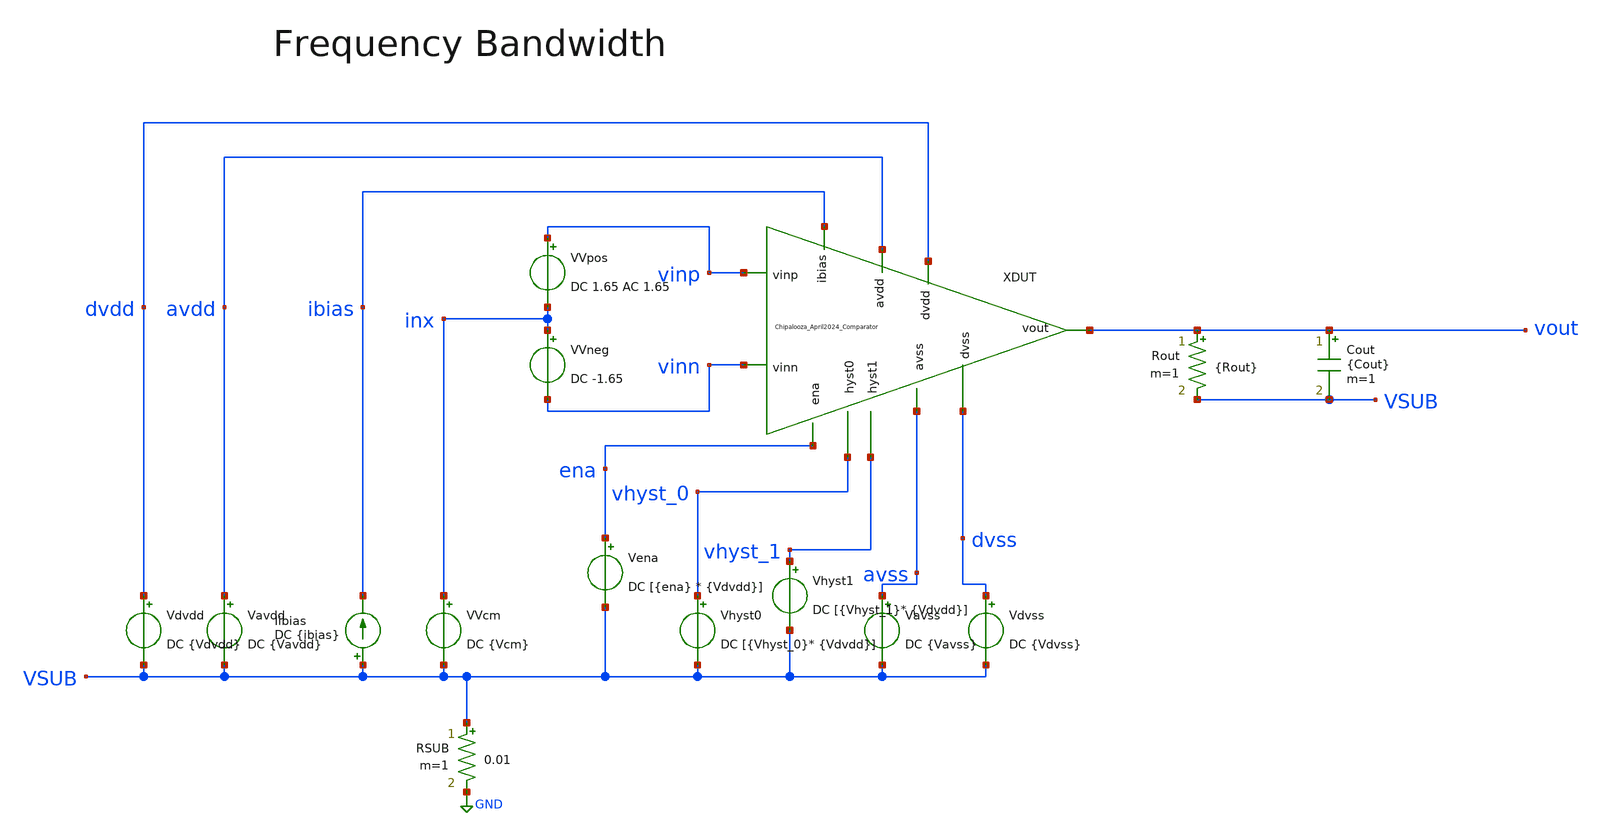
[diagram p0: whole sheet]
** sch_path: Chipalooza_April2024_Comparator/xschem/TB_frequencyBandwidth.sch
**.subckt TB_frequencyBandwidth
Vavdd avdd VSUB DC {Vavdd}
Rout vout VSUB {Rout} m=1
Cout vout VSUB {Cout} m=1
Vdvdd dvdd VSUB DC {Vdvdd}
Vena ena VSUB DC [{ena} * {Vdvdd}]
Vhyst0 vhyst_0 VSUB DC [{Vhyst_0}* {Vdvdd}]
Vhyst1 vhyst_1 VSUB DC [{Vhyst_1}* {Vdvdd}]
Vavss avss VSUB DC {Vavss}
Vdvss dvss VSUB DC {Vdvss}
RSUB VSUB GND 0.01 m=1
Iibias VSUB ibias DC {ibias}
XDUT vhyst_0 vhyst_1 avdd vinp avss vinn dvdd dvss vout ibias ena Chipalooza_April2024_Comparator
VVpos vinp inx DC 1.65 AC 1.65
VVneg inx vinn DC -1.65
VVcm inx VSUB DC {Vcm}
**** begin user architecture code

.control

ac dec 20 1 1e12
plot v(vout)
plot v(dvdd)
plot v(avdd)

meas ac peak MAX vmag(vout) FROM=2 TO=1.5GHz
let f3db = peak/sqrt(2)
meas ac f1 when vmag(vout)=f3db RISE=1
meas ac f2 when vmag(vout)=f3db FALL=1

let f3 = $&f2
echo $&f3 > {simpath}/{filename}_{N}.data

write ngspice/frequencyBandwidth.raw

.endc



* CACE gensim simulation file {filename}_{N}
* Generated by CACE gensim, Efabless Corporation (c) 2023
* Find the current through the amplifier under condition of static input

.include {DUT_path}

.lib {PDK_ROOT}/{PDK}/libs.tech/combined/sky130.lib.spice {corner}

.option TEMP={temperature}
* Flag unsafe operating conditions (exceeds models' specified limits)
.option warn=1
.option savecurrents
.option save all


**** end user architecture code
**.ends

* expanding   symbol:  Chipalooza_April2024_Comparator.sym # of pins=11
** sym_path: Chipalooza_April2024_Comparator/xschem/Chipalooza_April2024_Comparator.sym
** sch_path: Chipalooza_April2024_Comparator/xschem/Chipalooza_April2024_Comparator.sch
.subckt Chipalooza_April2024_Comparator hyst0 hyst1 avdd vinp avss vinn dvdd dvss vout ibias ena
*.ipin vinp
*.ipin vinn
*.ipin hyst0
*.ipin hyst1
*.ipin avdd
*.ipin avss
*.ipin dvdd
*.ipin dvss
*.opin vout
*.ipin ena
*.ipin ibias
XM29 SumOutBar SumOut dvdd dvdd sky130_fd_pr__pfet_01v8 L=1 W=2 nf=1 ad='int((nf+1)/2) * W/nf * 0.29' as='int((nf+2)/2)
+ * W/nf * 0.29' pd='2*int((nf+1)/2) * (W/nf + 0.29)' ps='2*int((nf+2)/2) * (W/nf + 0.29)' nrd='0.29 /
+ W' nrs='0.29 / W' sa=0 sb=0 sd=0 mult=2 m=2
XM30 SumOutBar SumOut dvssi dvss sky130_fd_pr__nfet_01v8 L=1 W=2 nf=1 ad='int((nf+1)/2) * W/nf * 0.29' as='int((nf+2)/2)
+ * W/nf * 0.29' pd='2*int((nf+1)/2) * (W/nf + 0.29)' ps='2*int((nf+2)/2) * (W/nf + 0.29)' nrd='0.29 /
+ W' nrs='0.29 / W' sa=0 sb=0 sd=0 mult=2 m=2
XM25 net2 hyst_bias0 avss avss sky130_fd_pr__nfet_g5v0d10v5 L=1 W=3 nf=1 ad='int((nf+1)/2) * W/nf * 0.29' as='int((nf+2)/2)
+ * W/nf * 0.29' pd='2*int((nf+1)/2) * (W/nf + 0.29)' ps='2*int((nf+2)/2) * (W/nf + 0.29)' nrd='0.29 /
+ W' nrs='0.29 / W' sa=0 sb=0 sd=0 mult=2 m=2
XM26 hyst_bias0 ibias dvssi dvss sky130_fd_pr__nfet_01v8 L=1 W=3 nf=1 ad='int((1 + 1)/2) * 3 / 1 * 0.29' as='int((1
+ + 2)/2) * 3 / 1 * 0.29' pd='2*int((1 + 1)/2) * (3 / 1 + 0.29)' ps='2*int((1 + 2)/2) * (3 / 1 + 0.29)' nrd='0.29
+ / 3 ' nrs='0.29 / 3 ' sa=0 sb=0 sd=0 mult=2 m=2
XM27 ibias ibias dvssi dvss sky130_fd_pr__nfet_01v8 L=1 W=3 nf=1 ad='int((1 + 1)/2) * 3 / 1 * 0.29' as='int((1
+ + 2)/2) * 3 / 1 * 0.29' pd='2*int((1 + 1)/2) * (3 / 1 + 0.29)' ps='2*int((1 + 2)/2) * (3 / 1 + 0.29)' nrd='0.29
+ / 3 ' nrs='0.29 / 3 ' sa=0 sb=0 sd=0 mult=2 m=2
XM34 hyst_bias1 hyst_bias0 dvdd dvdd sky130_fd_pr__pfet_01v8 L=1 W=3 nf=1 ad='int((nf+1)/2) * W/nf *
+ 0.29' as='int((nf+2)/2) * W/nf * 0.29' pd='2*int((nf+1)/2) * (W/nf + 0.29)' ps='2*int((nf+2)/2) * (W/nf
+ + 0.29)' nrd='0.29 / W' nrs='0.29 / W' sa=0 sb=0 sd=0 mult=2 m=2
XM35 hyst_bias0 hyst_bias0 dvdd dvdd sky130_fd_pr__pfet_01v8 L=1 W=3 nf=1 ad='int((nf+1)/2) * W/nf *
+ 0.29' as='int((nf+2)/2) * W/nf * 0.29' pd='2*int((nf+1)/2) * (W/nf + 0.29)' ps='2*int((nf+2)/2) * (W/nf
+ + 0.29)' nrd='0.29 / W' nrs='0.29 / W' sa=0 sb=0 sd=0 mult=2 m=2
XM36 dvdd hyst_bias1 dvssi dvss sky130_fd_pr__nfet_01v8 L=1 W=3 nf=1 ad='int((1 + 1)/2) * 3 / 1 * 0.29' as='int((1
+ + 2)/2) * 3 / 1 * 0.29' pd='2*int((1 + 1)/2) * (3 / 1 + 0.29)' ps='2*int((1 + 2)/2) * (3 / 1 + 0.29)' nrd='0.29
+ / 3 ' nrs='0.29 / 3 ' sa=0 sb=0 sd=0 mult=2 m=2
XM37 hyst_bias1 hyst_bias1 dvssi dvss sky130_fd_pr__nfet_01v8 L=1 W=3 nf=1 ad='int((1 + 1)/2) * 3 / 1
+ * 0.29' as='int((1 + 2)/2) * 3 / 1 * 0.29' pd='2*int((1 + 1)/2) * (3 / 1 + 0.29)' ps='2*int((1 + 2)/2)
+ * (3 / 1 + 0.29)' nrd='0.29 / 3 ' nrs='0.29 / 3 ' sa=0 sb=0 sd=0 mult=2 m=2
C1 avss 0 2p m=1
XM38 avssi ena avss avss sky130_fd_pr__nfet_g5v0d10v5 L=1 W=16 nf=1 ad='int((nf+1)/2) * W/nf * 0.29' as='int((nf+2)/2)
+ * W/nf * 0.29' pd='2*int((nf+1)/2) * (W/nf + 0.29)' ps='2*int((nf+2)/2) * (W/nf + 0.29)' nrd='0.29 /
+ W' nrs='0.29 / W' sa=0 sb=0 sd=0 mult=2 m=2
XM39 net3 hyst_bias0 avss avss sky130_fd_pr__nfet_g5v0d10v5 L=1 W=8 nf=1 ad='int((nf+1)/2) * W/nf * 0.29' as='int((nf+2)/2)
+ * W/nf * 0.29' pd='2*int((nf+1)/2) * (W/nf + 0.29)' ps='2*int((nf+2)/2) * (W/nf + 0.29)' nrd='0.29 /
+ W' nrs='0.29 / W' sa=0 sb=0 sd=0 mult=4 m=4
XM40 net1 hyst0 net2 avss sky130_fd_pr__nfet_g5v0d10v5 L=1 W=3 nf=1 ad='int((nf+1)/2) * W/nf * 0.29' as='int((nf+2)/2)
+ * W/nf * 0.29' pd='2*int((nf+1)/2) * (W/nf + 0.29)' ps='2*int((nf+2)/2) * (W/nf + 0.29)' nrd='0.29 /
+ W' nrs='0.29 / W' sa=0 sb=0 sd=0 mult=2 m=2
XM41 net1 hyst1 net3 avss sky130_fd_pr__nfet_g5v0d10v5 L=1 W=8 nf=1 ad='int((nf+1)/2) * W/nf * 0.29' as='int((nf+2)/2)
+ * W/nf * 0.29' pd='2*int((nf+1)/2) * (W/nf + 0.29)' ps='2*int((nf+2)/2) * (W/nf + 0.29)' nrd='0.29 /
+ W' nrs='0.29 / W' sa=0 sb=0 sd=0 mult=4 m=4
C2 avss 0 2p m=1
XM13 dvssi ena avss avss sky130_fd_pr__nfet_g5v0d10v5 L=1 W=16 nf=1 ad='int((nf+1)/2) * W/nf * 0.29' as='int((nf+2)/2)
+ * W/nf * 0.29' pd='2*int((nf+1)/2) * (W/nf + 0.29)' ps='2*int((nf+2)/2) * (W/nf + 0.29)' nrd='0.29 /
+ W' nrs='0.29 / W' sa=0 sb=0 sd=0 mult=2 m=2
XM16 vout SumOutBar dvdd dvdd sky130_fd_pr__pfet_01v8 L=1 W=2 nf=1 ad='int((nf+1)/2) * W/nf * 0.29' as='int((nf+2)/2)
+ * W/nf * 0.29' pd='2*int((nf+1)/2) * (W/nf + 0.29)' ps='2*int((nf+2)/2) * (W/nf + 0.29)' nrd='0.29 /
+ W' nrs='0.29 / W' sa=0 sb=0 sd=0 mult=2 m=2
XM18 vout SumOutBar dvssi dvss sky130_fd_pr__nfet_01v8 L=1 W=2 nf=1 ad='int((nf+1)/2) * W/nf * 0.29' as='int((nf+2)/2)
+ * W/nf * 0.29' pd='2*int((nf+1)/2) * (W/nf + 0.29)' ps='2*int((nf+2)/2) * (W/nf + 0.29)' nrd='0.29 /
+ W' nrs='0.29 / W' sa=0 sb=0 sd=0 mult=2 m=2
XM19 net14 SumOutBar net15 dvdd sky130_fd_pr__pfet_01v8 L=1 W=2 nf=1 ad='int((nf+1)/2) * W/nf * 0.29' as='int((nf+2)/2)
+ * W/nf * 0.29' pd='2*int((nf+1)/2) * (W/nf + 0.29)' ps='2*int((nf+2)/2) * (W/nf + 0.29)' nrd='0.29 /
+ W' nrs='0.29 / W' sa=0 sb=0 sd=0 mult=2 m=2
XM24 net1 SumOut N2 dvdd sky130_fd_pr__pfet_01v8 L=1 W=2 nf=1 ad='int((nf+1)/2) * W/nf * 0.29' as='int((nf+2)/2)
+ * W/nf * 0.29' pd='2*int((nf+1)/2) * (W/nf + 0.29)' ps='2*int((nf+2)/2) * (W/nf + 0.29)' nrd='0.29 /
+ W' nrs='0.29 / W' sa=0 sb=0 sd=0 mult=2 m=2
XM4 SourceBias2 SourceBias2 avdd avdd sky130_fd_pr__pfet_g5v0d10v5 L=1 W=2 nf=1 ad='int((nf+1)/2) * W/nf
+ * 0.29' as='int((nf+2)/2) * W/nf * 0.29' pd='2*int((nf+1)/2) * (W/nf + 0.29)' ps='2*int((nf+2)/2) * (W/nf
+ + 0.29)' nrd='0.29 / W' nrs='0.29 / W' sa=0 sb=0 sd=0 mult=2 m=2
XM5 N1 SourceBias2 avdd avdd sky130_fd_pr__pfet_g5v0d10v5 L=1 W=2 nf=1 ad='int((nf+1)/2) * W/nf * 0.29' as='int((nf+2)/2)
+ * W/nf * 0.29' pd='2*int((nf+1)/2) * (W/nf + 0.29)' ps='2*int((nf+2)/2) * (W/nf + 0.29)' nrd='0.29 /
+ W' nrs='0.29 / W' sa=0 sb=0 sd=0 mult=2 m=2
XM6 N2 SourceBias2 avdd avdd sky130_fd_pr__pfet_g5v0d10v5 L=1 W=2 nf=1 ad='int((nf+1)/2) * W/nf * 0.29' as='int((nf+2)/2)
+ * W/nf * 0.29' pd='2*int((nf+1)/2) * (W/nf + 0.29)' ps='2*int((nf+2)/2) * (W/nf + 0.29)' nrd='0.29 /
+ W' nrs='0.29 / W' sa=0 sb=0 sd=0 mult=2 m=2
XM7 SumOut Bias1 N2 avdd sky130_fd_pr__pfet_g5v0d10v5 L=1 W=2 nf=1 ad='int((nf+1)/2) * W/nf * 0.29' as='int((nf+2)/2)
+ * W/nf * 0.29' pd='2*int((nf+1)/2) * (W/nf + 0.29)' ps='2*int((nf+2)/2) * (W/nf + 0.29)' nrd='0.29 /
+ W' nrs='0.29 / W' sa=0 sb=0 sd=0 mult=2 m=2
XM8 Sum Bias1 N1 avdd sky130_fd_pr__pfet_g5v0d10v5 L=1 W=2 nf=1 ad='int((nf+1)/2) * W/nf * 0.29' as='int((nf+2)/2)
+ * W/nf * 0.29' pd='2*int((nf+1)/2) * (W/nf + 0.29)' ps='2*int((nf+2)/2) * (W/nf + 0.29)' nrd='0.29 /
+ W' nrs='0.29 / W' sa=0 sb=0 sd=0 mult=2 m=2
XM9 SumOut Bias2 P2 avss sky130_fd_pr__nfet_g5v0d10v5 L=1 W=2 nf=1 ad='int((nf+1)/2) * W/nf * 0.29' as='int((nf+2)/2)
+ * W/nf * 0.29' pd='2*int((nf+1)/2) * (W/nf + 0.29)' ps='2*int((nf+2)/2) * (W/nf + 0.29)' nrd='0.29 /
+ W' nrs='0.29 / W' sa=0 sb=0 sd=0 mult=2 m=2
XM10 Sum Bias2 P1 avss sky130_fd_pr__nfet_g5v0d10v5 L=1 W=2 nf=1 ad='int((nf+1)/2) * W/nf * 0.29' as='int((nf+2)/2)
+ * W/nf * 0.29' pd='2*int((nf+1)/2) * (W/nf + 0.29)' ps='2*int((nf+2)/2) * (W/nf + 0.29)' nrd='0.29 /
+ W' nrs='0.29 / W' sa=0 sb=0 sd=0 mult=2 m=2
XM11 P2 Sum avss avss sky130_fd_pr__nfet_g5v0d10v5 L=1 W=2 nf=1 ad='int((nf+1)/2) * W/nf * 0.29' as='int((nf+2)/2)
+ * W/nf * 0.29' pd='2*int((nf+1)/2) * (W/nf + 0.29)' ps='2*int((nf+2)/2) * (W/nf + 0.29)' nrd='0.29 /
+ W' nrs='0.29 / W' sa=0 sb=0 sd=0 mult=2 m=2
XM12 P1 Sum avss avss sky130_fd_pr__nfet_g5v0d10v5 L=1 W=2 nf=1 ad='int((nf+1)/2) * W/nf * 0.29' as='int((nf+2)/2)
+ * W/nf * 0.29' pd='2*int((nf+1)/2) * (W/nf + 0.29)' ps='2*int((nf+2)/2) * (W/nf + 0.29)' nrd='0.29 /
+ W' nrs='0.29 / W' sa=0 sb=0 sd=0 mult=2 m=2
XM2 P2 vinn psource_input avdd sky130_fd_pr__pfet_g5v0d10v5 L=1 W=4 nf=1 ad='int((nf+1)/2) * W/nf * 0.29' as='int((nf+2)/2)
+ * W/nf * 0.29' pd='2*int((nf+1)/2) * (W/nf + 0.29)' ps='2*int((nf+2)/2) * (W/nf + 0.29)' nrd='0.29 /
+ W' nrs='0.29 / W' sa=0 sb=0 sd=0 mult=2 m=2
XM3 P1 vinp psource_input avdd sky130_fd_pr__pfet_g5v0d10v5 L=1 W=4 nf=1 ad='int((nf+1)/2) * W/nf * 0.29' as='int((nf+2)/2)
+ * W/nf * 0.29' pd='2*int((nf+1)/2) * (W/nf + 0.29)' ps='2*int((nf+2)/2) * (W/nf + 0.29)' nrd='0.29 /
+ W' nrs='0.29 / W' sa=0 sb=0 sd=0 mult=2 m=2
XM14 psource_input net4 avdd avdd sky130_fd_pr__pfet_g5v0d10v5 L=1 W=12 nf=1 ad='int((nf+1)/2) * W/nf
+ * 0.29' as='int((nf+2)/2) * W/nf * 0.29' pd='2*int((nf+1)/2) * (W/nf + 0.29)' ps='2*int((nf+2)/2) * (W/nf
+ + 0.29)' nrd='0.29 / W' nrs='0.29 / W' sa=0 sb=0 sd=0 mult=4 m=4
XM15 net4 net4 avdd avdd sky130_fd_pr__pfet_g5v0d10v5 L=1 W=8 nf=1 ad='int((nf+1)/2) * W/nf * 0.29' as='int((nf+2)/2)
+ * W/nf * 0.29' pd='2*int((nf+1)/2) * (W/nf + 0.29)' ps='2*int((nf+2)/2) * (W/nf + 0.29)' nrd='0.29 /
+ W' nrs='0.29 / W' sa=0 sb=0 sd=0 mult=2 m=2
XM17 nbias_tail net6 psource_input avdd sky130_fd_pr__pfet_g5v0d10v5 L=1 W=8 nf=1 ad='int((nf+1)/2) *
+ W/nf * 0.29' as='int((nf+2)/2) * W/nf * 0.29' pd='2*int((nf+1)/2) * (W/nf + 0.29)' ps='2*int((nf+2)/2)
+ * (W/nf + 0.29)' nrd='0.29 / W' nrs='0.29 / W' sa=0 sb=0 sd=0 mult=2 m=2
XM20 N1 vinp SourceBias0 avss sky130_fd_pr__nfet_g5v0d10v5 L=4 W=16 nf=1 ad='int((nf+1)/2) * W/nf * 0.29' as='int((nf+2)/2)
+ * W/nf * 0.29' pd='2*int((nf+1)/2) * (W/nf + 0.29)' ps='2*int((nf+2)/2) * (W/nf + 0.29)' nrd='0.29 /
+ W' nrs='0.29 / W' sa=0 sb=0 sd=0 mult=2 m=2
XM21 N2 vinn SourceBias0 avss sky130_fd_pr__nfet_g5v0d10v5 L=4 W=16 nf=1 ad='int((nf+1)/2) * W/nf * 0.29' as='int((nf+2)/2)
+ * W/nf * 0.29' pd='2*int((nf+1)/2) * (W/nf + 0.29)' ps='2*int((nf+2)/2) * (W/nf + 0.29)' nrd='0.29 /
+ W' nrs='0.29 / W' sa=0 sb=0 sd=0 mult=2 m=2
XM22 SourceBias0 nbias_tail avssi avss sky130_fd_pr__nfet_g5v0d10v5 L=1 W=12 nf=1 ad='int((nf+1)/2) *
+ W/nf * 0.29' as='int((nf+2)/2) * W/nf * 0.29' pd='2*int((nf+1)/2) * (W/nf + 0.29)' ps='2*int((nf+2)/2)
+ * (W/nf + 0.29)' nrd='0.29 / W' nrs='0.29 / W' sa=0 sb=0 sd=0 mult=4 m=4
XM23 nbias_tail nbias_tail avssi avss sky130_fd_pr__nfet_g5v0d10v5 L=1 W=12 nf=1 ad='int((nf+1)/2) *
+ W/nf * 0.29' as='int((nf+2)/2) * W/nf * 0.29' pd='2*int((nf+1)/2) * (W/nf + 0.29)' ps='2*int((nf+2)/2)
+ * (W/nf + 0.29)' nrd='0.29 / W' nrs='0.29 / W' sa=0 sb=0 sd=0 mult=2 m=2
XM28 net4 Bias5 SourceBias0 avss sky130_fd_pr__nfet_g5v0d10v5 L=1 W=4 nf=1 ad='int((nf+1)/2) * W/nf *
+ 0.29' as='int((nf+2)/2) * W/nf * 0.29' pd='2*int((nf+1)/2) * (W/nf + 0.29)' ps='2*int((nf+2)/2) * (W/nf
+ + 0.29)' nrd='0.29 / W' nrs='0.29 / W' sa=0 sb=0 sd=0 mult=2 m=2
XM31 SourceBias0 net5 avssi avss sky130_fd_pr__nfet_g5v0d10v5 L=4 W=16 nf=1 ad='int((nf+1)/2) * W/nf
+ * 0.29' as='int((nf+2)/2) * W/nf * 0.29' pd='2*int((nf+1)/2) * (W/nf + 0.29)' ps='2*int((nf+2)/2) * (W/nf
+ + 0.29)' nrd='0.29 / W' nrs='0.29 / W' sa=0 sb=0 sd=0 mult=2 m=2
XM44 net5 net5 avssi avss sky130_fd_pr__nfet_g5v0d10v5 L=4 W=16 nf=1 ad='int((nf+1)/2) * W/nf * 0.29' as='int((nf+2)/2)
+ * W/nf * 0.29' pd='2*int((nf+1)/2) * (W/nf + 0.29)' ps='2*int((nf+2)/2) * (W/nf + 0.29)' nrd='0.29 /
+ W' nrs='0.29 / W' sa=0 sb=0 sd=0 mult=2 m=2
XM45 SourceBias1 net5 avssi avss sky130_fd_pr__nfet_g5v0d10v5 L=4 W=16 nf=1 ad='int((nf+1)/2) * W/nf
+ * 0.29' as='int((nf+2)/2) * W/nf * 0.29' pd='2*int((nf+1)/2) * (W/nf + 0.29)' ps='2*int((nf+2)/2) * (W/nf
+ + 0.29)' nrd='0.29 / W' nrs='0.29 / W' sa=0 sb=0 sd=0 mult=2 m=2
XM46 SourceBias1 SourceBias1 avdd avdd sky130_fd_pr__pfet_g5v0d10v5 L=1 W=12 nf=1 ad='int((nf+1)/2) *
+ W/nf * 0.29' as='int((nf+2)/2) * W/nf * 0.29' pd='2*int((nf+1)/2) * (W/nf + 0.29)' ps='2*int((nf+2)/2)
+ * (W/nf + 0.29)' nrd='0.29 / W' nrs='0.29 / W' sa=0 sb=0 sd=0 mult=4 m=4
XM47 psource_input SourceBias1 avdd avdd sky130_fd_pr__pfet_g5v0d10v5 L=1 W=12 nf=1 ad='int((nf+1)/2)
+ * W/nf * 0.29' as='int((nf+2)/2) * W/nf * 0.29' pd='2*int((nf+1)/2) * (W/nf + 0.29)' ps='2*int((nf+2)/2)
+ * (W/nf + 0.29)' nrd='0.29 / W' nrs='0.29 / W' sa=0 sb=0 sd=0 mult=4 m=4
XM48 SourceBias2 net5 avssi avss sky130_fd_pr__nfet_g5v0d10v5 L=4 W=16 nf=1 ad='int((nf+1)/2) * W/nf
+ * 0.29' as='int((nf+2)/2) * W/nf * 0.29' pd='2*int((nf+1)/2) * (W/nf + 0.29)' ps='2*int((nf+2)/2) * (W/nf
+ + 0.29)' nrd='0.29 / W' nrs='0.29 / W' sa=0 sb=0 sd=0 mult=4 m=4
XM63 net6 net6 avdd avdd sky130_fd_pr__pfet_g5v0d10v5 L=5 W=3 nf=1 ad='int((nf+1)/2) * W/nf * 0.29' as='int((nf+2)/2)
+ * W/nf * 0.29' pd='2*int((nf+1)/2) * (W/nf + 0.29)' ps='2*int((nf+2)/2) * (W/nf + 0.29)' nrd='0.29 /
+ W' nrs='0.29 / W' sa=0 sb=0 sd=0 mult=1 m=1
XM62 avdd Bias4 SourceBias3 avss sky130_fd_pr__nfet_g5v0d10v5 L=1 W=4 nf=1 ad='int((nf+1)/2) * W/nf *
+ 0.29' as='int((nf+2)/2) * W/nf * 0.29' pd='2*int((nf+1)/2) * (W/nf + 0.29)' ps='2*int((nf+2)/2) * (W/nf
+ + 0.29)' nrd='0.29 / W' nrs='0.29 / W' sa=0 sb=0 sd=0 mult=2 m=2
XM64 net6 Bias4 SourceBias3 avss sky130_fd_pr__nfet_g5v0d10v5 L=1 W=4 nf=1 ad='int((nf+1)/2) * W/nf *
+ 0.29' as='int((nf+2)/2) * W/nf * 0.29' pd='2*int((nf+1)/2) * (W/nf + 0.29)' ps='2*int((nf+2)/2) * (W/nf
+ + 0.29)' nrd='0.29 / W' nrs='0.29 / W' sa=0 sb=0 sd=0 mult=2 m=2
XM65 SourceBias3 net5 avssi avss sky130_fd_pr__nfet_g5v0d10v5 L=4 W=16 nf=1 ad='int((nf+1)/2) * W/nf
+ * 0.29' as='int((nf+2)/2) * W/nf * 0.29' pd='2*int((nf+1)/2) * (W/nf + 0.29)' ps='2*int((nf+2)/2) * (W/nf
+ + 0.29)' nrd='0.29 / W' nrs='0.29 / W' sa=0 sb=0 sd=0 mult=4 m=4
XM76 Bias1 net5 avssi avss sky130_fd_pr__nfet_g5v0d10v5 L=4 W=16 nf=1 ad='int((nf+1)/2) * W/nf * 0.29' as='int((nf+2)/2)
+ * W/nf * 0.29' pd='2*int((nf+1)/2) * (W/nf + 0.29)' ps='2*int((nf+2)/2) * (W/nf + 0.29)' nrd='0.29 /
+ W' nrs='0.29 / W' sa=0 sb=0 sd=0 mult=4 m=4
XM77 SourceBias5 net5 avssi avss sky130_fd_pr__nfet_g5v0d10v5 L=4 W=16 nf=1 ad='int((nf+1)/2) * W/nf
+ * 0.29' as='int((nf+2)/2) * W/nf * 0.29' pd='2*int((nf+1)/2) * (W/nf + 0.29)' ps='2*int((nf+2)/2) * (W/nf
+ + 0.29)' nrd='0.29 / W' nrs='0.29 / W' sa=0 sb=0 sd=0 mult=4 m=4
XM78 SourceBias6 net5 avssi avss sky130_fd_pr__nfet_g5v0d10v5 L=4 W=16 nf=1 ad='int((nf+1)/2) * W/nf
+ * 0.29' as='int((nf+2)/2) * W/nf * 0.29' pd='2*int((nf+1)/2) * (W/nf + 0.29)' ps='2*int((nf+2)/2) * (W/nf
+ + 0.29)' nrd='0.29 / W' nrs='0.29 / W' sa=0 sb=0 sd=0 mult=4 m=4
XM79 SourceBias7 net5 avssi avss sky130_fd_pr__nfet_g5v0d10v5 L=4 W=16 nf=1 ad='int((nf+1)/2) * W/nf
+ * 0.29' as='int((nf+2)/2) * W/nf * 0.29' pd='2*int((nf+1)/2) * (W/nf + 0.29)' ps='2*int((nf+2)/2) * (W/nf
+ + 0.29)' nrd='0.29 / W' nrs='0.29 / W' sa=0 sb=0 sd=0 mult=4 m=4
XM81 Bias5 net5 avssi avss sky130_fd_pr__nfet_g5v0d10v5 L=4 W=16 nf=1 ad='int((nf+1)/2) * W/nf * 0.29' as='int((nf+2)/2)
+ * W/nf * 0.29' pd='2*int((nf+1)/2) * (W/nf + 0.29)' ps='2*int((nf+2)/2) * (W/nf + 0.29)' nrd='0.29 /
+ W' nrs='0.29 / W' sa=0 sb=0 sd=0 mult=4 m=4
XM82 Bias4 net5 avssi avss sky130_fd_pr__nfet_g5v0d10v5 L=4 W=16 nf=1 ad='int((nf+1)/2) * W/nf * 0.29' as='int((nf+2)/2)
+ * W/nf * 0.29' pd='2*int((nf+1)/2) * (W/nf + 0.29)' ps='2*int((nf+2)/2) * (W/nf + 0.29)' nrd='0.29 /
+ W' nrs='0.29 / W' sa=0 sb=0 sd=0 mult=4 m=4
XM83 SourceBias10 net5 avssi avss sky130_fd_pr__nfet_g5v0d10v5 L=4 W=16 nf=1 ad='int((nf+1)/2) * W/nf
+ * 0.29' as='int((nf+2)/2) * W/nf * 0.29' pd='2*int((nf+1)/2) * (W/nf + 0.29)' ps='2*int((nf+2)/2) * (W/nf
+ + 0.29)' nrd='0.29 / W' nrs='0.29 / W' sa=0 sb=0 sd=0 mult=4 m=4
XM1 ibias ibias avssi avss sky130_fd_pr__nfet_g5v0d10v5 L=4 W=16 nf=1 ad='int((nf+1)/2) * W/nf * 0.29' as='int((nf+2)/2)
+ * W/nf * 0.29' pd='2*int((nf+1)/2) * (W/nf + 0.29)' ps='2*int((nf+2)/2) * (W/nf + 0.29)' nrd='0.29 /
+ W' nrs='0.29 / W' sa=0 sb=0 sd=0 mult=2 m=2
XM32 net7 ibias avssi avss sky130_fd_pr__nfet_g5v0d10v5 L=4 W=16 nf=1 ad='int((nf+1)/2) * W/nf * 0.29' as='int((nf+2)/2)
+ * W/nf * 0.29' pd='2*int((nf+1)/2) * (W/nf + 0.29)' ps='2*int((nf+2)/2) * (W/nf + 0.29)' nrd='0.29 /
+ W' nrs='0.29 / W' sa=0 sb=0 sd=0 mult=2 m=2
XM33 net7 net7 avdd avdd sky130_fd_pr__pfet_g5v0d10v5 L=1 W=8 nf=1 ad='int((nf+1)/2) * W/nf * 0.29' as='int((nf+2)/2)
+ * W/nf * 0.29' pd='2*int((nf+1)/2) * (W/nf + 0.29)' ps='2*int((nf+2)/2) * (W/nf + 0.29)' nrd='0.29 /
+ W' nrs='0.29 / W' sa=0 sb=0 sd=0 mult=2 m=2
XM42 net5 net7 avdd avdd sky130_fd_pr__pfet_g5v0d10v5 L=1 W=8 nf=1 ad='int((nf+1)/2) * W/nf * 0.29' as='int((nf+2)/2)
+ * W/nf * 0.29' pd='2*int((nf+1)/2) * (W/nf + 0.29)' ps='2*int((nf+2)/2) * (W/nf + 0.29)' nrd='0.29 /
+ W' nrs='0.29 / W' sa=0 sb=0 sd=0 mult=2 m=2
XM54 M55Source M55Drain avss avss sky130_fd_pr__nfet_g5v0d10v5 L=1.5 W=6 nf=1 ad='int((nf+1)/2) * W/nf
+ * 0.29' as='int((nf+2)/2) * W/nf * 0.29' pd='2*int((nf+1)/2) * (W/nf + 0.29)' ps='2*int((nf+2)/2) * (W/nf
+ + 0.29)' nrd='0.29 / W' nrs='0.29 / W' sa=0 sb=0 sd=0 mult=2 m=2
XM55 M55Drain Bias2 M55Source avss sky130_fd_pr__nfet_g5v0d10v5 L=1 W=9 nf=1 ad='int((nf+1)/2) * W/nf
+ * 0.29' as='int((nf+2)/2) * W/nf * 0.29' pd='2*int((nf+1)/2) * (W/nf + 0.29)' ps='2*int((nf+2)/2) * (W/nf
+ + 0.29)' nrd='0.29 / W' nrs='0.29 / W' sa=0 sb=0 sd=0 mult=2 m=2
XM56 Bias2 Bias2 avss avss sky130_fd_pr__nfet_g5v0d10v5 L=2 W=0.5 nf=1 ad='int((nf+1)/2) * W/nf * 0.29' as='int((nf+2)/2)
+ * W/nf * 0.29' pd='2*int((nf+1)/2) * (W/nf + 0.29)' ps='2*int((nf+2)/2) * (W/nf + 0.29)' nrd='0.29 /
+ W' nrs='0.29 / W' sa=0 sb=0 sd=0 mult=1 m=1
XM51 net8 net9 avdd avdd sky130_fd_pr__pfet_g5v0d10v5 L=2 W=20 nf=1 ad='int((nf+1)/2) * W/nf * 0.29' as='int((nf+2)/2)
+ * W/nf * 0.29' pd='2*int((nf+1)/2) * (W/nf + 0.29)' ps='2*int((nf+2)/2) * (W/nf + 0.29)' nrd='0.29 /
+ W' nrs='0.29 / W' sa=0 sb=0 sd=0 mult=2 m=2
XM49 net9 net9 avdd avdd sky130_fd_pr__pfet_g5v0d10v5 L=2 W=10 nf=1 ad='int((nf+1)/2) * W/nf * 0.29' as='int((nf+2)/2)
+ * W/nf * 0.29' pd='2*int((nf+1)/2) * (W/nf + 0.29)' ps='2*int((nf+2)/2) * (W/nf + 0.29)' nrd='0.29 /
+ W' nrs='0.29 / W' sa=0 sb=0 sd=0 mult=2 m=2
XM50 SourceBias4 SourceBias4 net9 avdd sky130_fd_pr__pfet_g5v0d10v5 L=1 W=10 nf=1 ad='int((nf+1)/2) *
+ W/nf * 0.29' as='int((nf+2)/2) * W/nf * 0.29' pd='2*int((nf+1)/2) * (W/nf + 0.29)' ps='2*int((nf+2)/2)
+ * (W/nf + 0.29)' nrd='0.29 / W' nrs='0.29 / W' sa=0 sb=0 sd=0 mult=2 m=2
XM52 avss SourceBias4 net8 avdd sky130_fd_pr__pfet_g5v0d10v5 L=1 W=1 nf=1 ad='int((nf+1)/2) * W/nf *
+ 0.29' as='int((nf+2)/2) * W/nf * 0.29' pd='2*int((nf+1)/2) * (W/nf + 0.29)' ps='2*int((nf+2)/2) * (W/nf
+ + 0.29)' nrd='0.29 / W' nrs='0.29 / W' sa=0 sb=0 sd=0 mult=2 m=2
XM53 Bias1 Bias1 net8 avdd sky130_fd_pr__pfet_g5v0d10v5 L=1 W=10 nf=1 ad='int((nf+1)/2) * W/nf * 0.29' as='int((nf+2)/2)
+ * W/nf * 0.29' pd='2*int((nf+1)/2) * (W/nf + 0.29)' ps='2*int((nf+2)/2) * (W/nf + 0.29)' nrd='0.29 /
+ W' nrs='0.29 / W' sa=0 sb=0 sd=0 mult=2 m=2
XM57 net10 net11 avdd avdd sky130_fd_pr__pfet_g5v0d10v5 L=2 W=20 nf=1 ad='int((nf+1)/2) * W/nf * 0.29' as='int((nf+2)/2)
+ * W/nf * 0.29' pd='2*int((nf+1)/2) * (W/nf + 0.29)' ps='2*int((nf+2)/2) * (W/nf + 0.29)' nrd='0.29 /
+ W' nrs='0.29 / W' sa=0 sb=0 sd=0 mult=2 m=2
XM58 net11 net11 avdd avdd sky130_fd_pr__pfet_g5v0d10v5 L=2 W=10 nf=1 ad='int((nf+1)/2) * W/nf * 0.29' as='int((nf+2)/2)
+ * W/nf * 0.29' pd='2*int((nf+1)/2) * (W/nf + 0.29)' ps='2*int((nf+2)/2) * (W/nf + 0.29)' nrd='0.29 /
+ W' nrs='0.29 / W' sa=0 sb=0 sd=0 mult=2 m=2
XM59 SourceBias10 SourceBias10 net11 avdd sky130_fd_pr__pfet_g5v0d10v5 L=1 W=10 nf=1 ad='int((nf+1)/2)
+ * W/nf * 0.29' as='int((nf+2)/2) * W/nf * 0.29' pd='2*int((nf+1)/2) * (W/nf + 0.29)' ps='2*int((nf+2)/2)
+ * (W/nf + 0.29)' nrd='0.29 / W' nrs='0.29 / W' sa=0 sb=0 sd=0 mult=2 m=2
XM60 avss SourceBias10 net10 avdd sky130_fd_pr__pfet_g5v0d10v5 L=1 W=1 nf=1 ad='int((nf+1)/2) * W/nf
+ * 0.29' as='int((nf+2)/2) * W/nf * 0.29' pd='2*int((nf+1)/2) * (W/nf + 0.29)' ps='2*int((nf+2)/2) * (W/nf
+ + 0.29)' nrd='0.29 / W' nrs='0.29 / W' sa=0 sb=0 sd=0 mult=2 m=2
XM61 Bias4 Bias4 net10 avdd sky130_fd_pr__pfet_g5v0d10v5 L=1 W=5 nf=1 ad='int((nf+1)/2) * W/nf * 0.29' as='int((nf+2)/2)
+ * W/nf * 0.29' pd='2*int((nf+1)/2) * (W/nf + 0.29)' ps='2*int((nf+2)/2) * (W/nf + 0.29)' nrd='0.29 /
+ W' nrs='0.29 / W' sa=0 sb=0 sd=0 mult=2 m=2
XM66 net12 net13 avdd avdd sky130_fd_pr__pfet_g5v0d10v5 L=2 W=20 nf=1 ad='int((nf+1)/2) * W/nf * 0.29' as='int((nf+2)/2)
+ * W/nf * 0.29' pd='2*int((nf+1)/2) * (W/nf + 0.29)' ps='2*int((nf+2)/2) * (W/nf + 0.29)' nrd='0.29 /
+ W' nrs='0.29 / W' sa=0 sb=0 sd=0 mult=2 m=2
XM67 net13 net13 avdd avdd sky130_fd_pr__pfet_g5v0d10v5 L=2 W=20 nf=1 ad='int((nf+1)/2) * W/nf * 0.29' as='int((nf+2)/2)
+ * W/nf * 0.29' pd='2*int((nf+1)/2) * (W/nf + 0.29)' ps='2*int((nf+2)/2) * (W/nf + 0.29)' nrd='0.29 /
+ W' nrs='0.29 / W' sa=0 sb=0 sd=0 mult=2 m=2
XM68 SourceBias7 SourceBias7 net13 avdd sky130_fd_pr__pfet_g5v0d10v5 L=1 W=10 nf=1 ad='int((nf+1)/2)
+ * W/nf * 0.29' as='int((nf+2)/2) * W/nf * 0.29' pd='2*int((nf+1)/2) * (W/nf + 0.29)' ps='2*int((nf+2)/2)
+ * (W/nf + 0.29)' nrd='0.29 / W' nrs='0.29 / W' sa=0 sb=0 sd=0 mult=2 m=2
XM69 avss SourceBias7 net12 avdd sky130_fd_pr__pfet_g5v0d10v5 L=1 W=1 nf=1 ad='int((nf+1)/2) * W/nf *
+ 0.29' as='int((nf+2)/2) * W/nf * 0.29' pd='2*int((nf+1)/2) * (W/nf + 0.29)' ps='2*int((nf+2)/2) * (W/nf
+ + 0.29)' nrd='0.29 / W' nrs='0.29 / W' sa=0 sb=0 sd=0 mult=2 m=2
XM70 Bias5 Bias5 net12 avdd sky130_fd_pr__pfet_g5v0d10v5 L=1 W=5 nf=1 ad='int((nf+1)/2) * W/nf * 0.29' as='int((nf+2)/2)
+ * W/nf * 0.29' pd='2*int((nf+1)/2) * (W/nf + 0.29)' ps='2*int((nf+2)/2) * (W/nf + 0.29)' nrd='0.29 /
+ W' nrs='0.29 / W' sa=0 sb=0 sd=0 mult=2 m=2
XM72 SourceBias5 SourceBias5 avdd avdd sky130_fd_pr__pfet_g5v0d10v5 L=1 W=12 nf=1 ad='int((nf+1)/2) *
+ W/nf * 0.29' as='int((nf+2)/2) * W/nf * 0.29' pd='2*int((nf+1)/2) * (W/nf + 0.29)' ps='2*int((nf+2)/2)
+ * (W/nf + 0.29)' nrd='0.29 / W' nrs='0.29 / W' sa=0 sb=0 sd=0 mult=4 m=4
XM73 M55Drain SourceBias5 avdd avdd sky130_fd_pr__pfet_g5v0d10v5 L=1 W=12 nf=1 ad='int((nf+1)/2) * W/nf
+ * 0.29' as='int((nf+2)/2) * W/nf * 0.29' pd='2*int((nf+1)/2) * (W/nf + 0.29)' ps='2*int((nf+2)/2) * (W/nf
+ + 0.29)' nrd='0.29 / W' nrs='0.29 / W' sa=0 sb=0 sd=0 mult=4 m=4
XM74 SourceBias6 SourceBias6 avdd avdd sky130_fd_pr__pfet_g5v0d10v5 L=1 W=12 nf=1 ad='int((nf+1)/2) *
+ W/nf * 0.29' as='int((nf+2)/2) * W/nf * 0.29' pd='2*int((nf+1)/2) * (W/nf + 0.29)' ps='2*int((nf+2)/2)
+ * (W/nf + 0.29)' nrd='0.29 / W' nrs='0.29 / W' sa=0 sb=0 sd=0 mult=4 m=4
XM75 Bias2 SourceBias6 avdd avdd sky130_fd_pr__pfet_g5v0d10v5 L=1 W=12 nf=1 ad='int((nf+1)/2) * W/nf
+ * 0.29' as='int((nf+2)/2) * W/nf * 0.29' pd='2*int((nf+1)/2) * (W/nf + 0.29)' ps='2*int((nf+2)/2) * (W/nf
+ + 0.29)' nrd='0.29 / W' nrs='0.29 / W' sa=0 sb=0 sd=0 mult=4 m=4
.ends

.GLOBAL GND
.end
